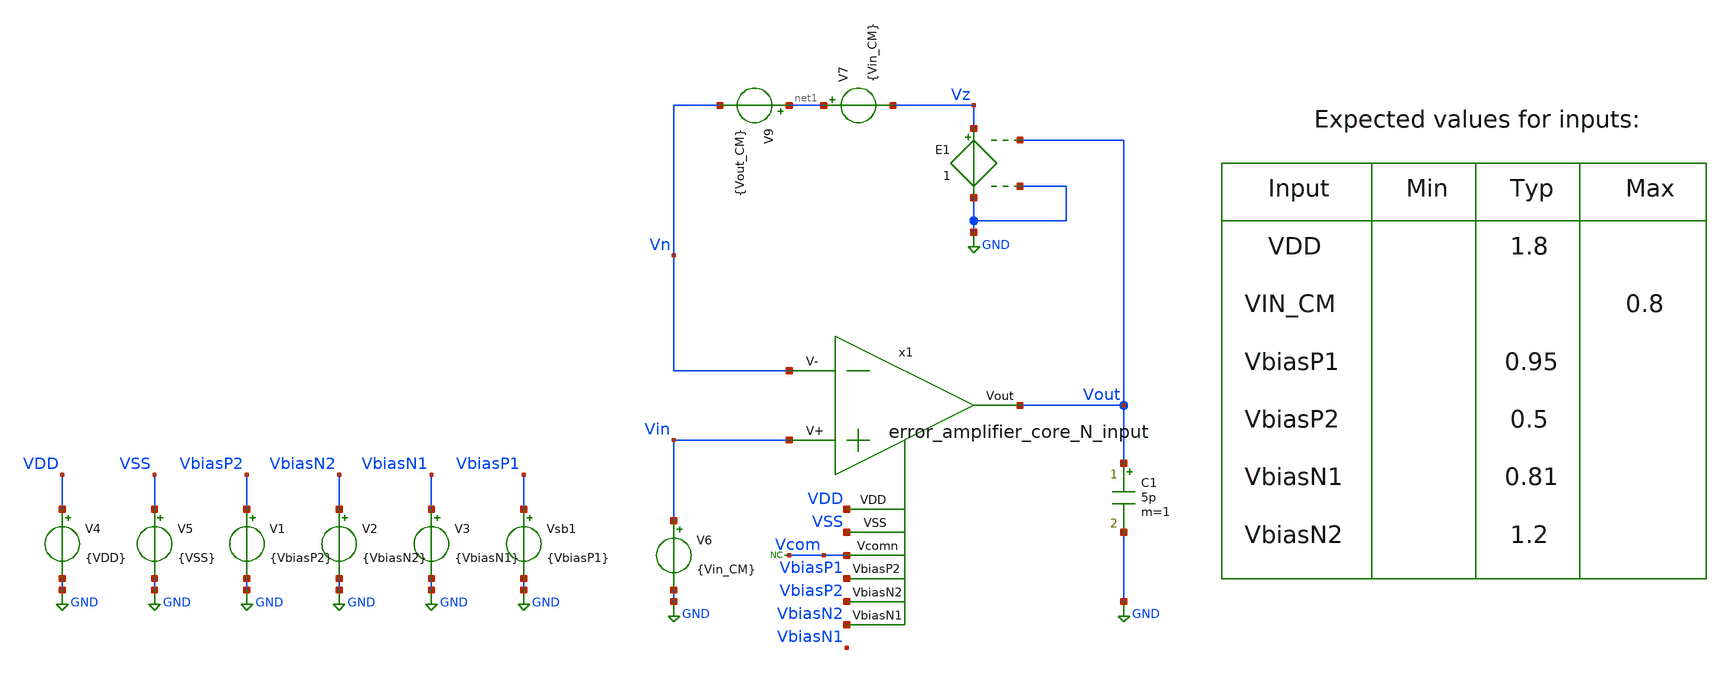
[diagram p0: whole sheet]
** sch_path: blocks/composite/folded_cascode/designs/gf180/error_amplifier_core_N_input/xschem/error_amplifier_core_Out_Swing.sch
**.subckt error_amplifier_core_Out_Swing
V1 VbiasP2 GND {VbiasP2}
V2 VbiasN2 GND {VbiasN2}
V3 VbiasN1 GND {VbiasN1}
V4 VDD GND {VDD}
V5 VSS GND {VSS}
C1 Vout GND 5p m=1
V6 Vin GND {Vin_CM}
x1 VbiasP1 VbiasP2 VbiasN2 Vout Vin Vn VDD VSS Vcom error_amplifier_core_N_input
Vsb1 VbiasP1 GND {VbiasP1}
V9 net1 Vn {Vout_CM}
E1 Vz GND Vout GND 1
* noconn Vcom
V7 net1 Vz {Vin_CM}
**** begin user architecture code




* --- Include PDK and Model Files ---
.include /foss/pdks/gf180mcuD/libs.tech/ngspice/design.ngspice
.lib /foss/pdks/gf180mcuD/libs.tech/ngspice/sm141064.ngspice typical

* --- Define Parameters for the Simulation ---
.param VDD = 1.8
.param VSS = 0
.param VbiasN1 = 0.81
.param VbiasN2 = 1.2
.param VbiasP1 = 0.95
.param VbiasP2 = 0.5
.param Vin_CM = 0.8
.param Vout_CM = 0.9
.param Vy = (Vout_CM - Vin_CM)
.param load_cap = 5*1e-12

* --- Simulation Commands and Analysis ---
.control
save all

** OP & DC simulations
op
dc V9 0 1.8 0.001

** DC measurements
setplot dc1
let dvout = deriv(v(Vout))

meas dc limmin when dvout=0.98 rise=1
meas dc limmax when dvout=0.98 fall=1

let Output_swing = limmax - limmin

print Output_swing
plot dvout


write error_amplifier_core_N_input_op.raw
.endc



**** end user architecture code
**.ends

* expanding   symbol:  gf180/error_amplifier_core_N_input/xschem/error_amplifier_core_N_input.sym #
*+ of pins=9
** sym_path: blocks/composite/folded_cascode/designs/gf180/error_amplifier_core_N_input/xschem/error_amplifier_core_N_input.sym
** sch_path: blocks/composite/folded_cascode/designs/gf180/error_amplifier_core_N_input/xschem/error_amplifier_core_N_input.sch
.subckt error_amplifier_core_N_input VbiasP2 VbiasN2 VbiasN1 Vout V+ V- VDD VSS Vcomn
*.ipin VbiasN2
*.iopin VDD
*.ipin VbiasP2
*.ipin VbiasN1
*.ipin V+
*.ipin V-
*.iopin VSS
*.iopin Vcomn
*.iopin Vout
XM4 Vdm6 Val VDD VDD pfet_03v3 L=0.3u W=4u nf=1 ad='int((nf+1)/2) * W/nf * 0.18u' as='int((nf+2)/2) * W/nf * 0.18u'
+ pd='2*int((nf+1)/2) * (W/nf + 0.18u)' ps='2*int((nf+2)/2) * (W/nf + 0.18u)' nrd='0.18u / W' nrs='0.18u / W'
+ sa=0 sb=0 sd=0 m=12
XM3 Vdm5 Val VDD VDD pfet_03v3 L=0.3u W=4u nf=1 ad='int((nf+1)/2) * W/nf * 0.18u' as='int((nf+2)/2) * W/nf * 0.18u'
+ pd='2*int((nf+1)/2) * (W/nf + 0.18u)' ps='2*int((nf+2)/2) * (W/nf + 0.18u)' nrd='0.18u / W' nrs='0.18u / W'
+ sa=0 sb=0 sd=0 m=12
XM5 Val VbiasP2 Vdm5 VDD pfet_03v3 L=2u W=6u nf=1 ad='int((nf+1)/2) * W/nf * 0.18u' as='int((nf+2)/2) * W/nf * 0.18u'
+ pd='2*int((nf+1)/2) * (W/nf + 0.18u)' ps='2*int((nf+2)/2) * (W/nf + 0.18u)' nrd='0.18u / W' nrs='0.18u / W'
+ sa=0 sb=0 sd=0 m=2
XM6 Vout VbiasP2 Vdm6 VDD pfet_03v3 L=2u W=6u nf=1 ad='int((nf+1)/2) * W/nf * 0.18u' as='int((nf+2)/2) * W/nf * 0.18u'
+ pd='2*int((nf+1)/2) * (W/nf + 0.18u)' ps='2*int((nf+2)/2) * (W/nf + 0.18u)' nrd='0.18u / W' nrs='0.18u / W'
+ sa=0 sb=0 sd=0 m=2
XM9 net1 VbiasN1 VSS VSS nfet_03v3 L=2u W=2u nf=1 ad='int((nf+1)/2) * W/nf * 0.18u' as='int((nf+2)/2) * W/nf * 0.18u'
+ pd='2*int((nf+1)/2) * (W/nf + 0.18u)' ps='2*int((nf+2)/2) * (W/nf + 0.18u)' nrd='0.18u / W' nrs='0.18u / W'
+ sa=0 sb=0 sd=0 m=2
XM8 Vout VbiasN2 Vcomn VSS nfet_03v3 L=2u W=5u nf=1 ad='int((nf+1)/2) * W/nf * 0.18u' as='int((nf+2)/2) * W/nf * 0.18u'
+ pd='2*int((nf+1)/2) * (W/nf + 0.18u)' ps='2*int((nf+2)/2) * (W/nf + 0.18u)' nrd='0.18u / W' nrs='0.18u / W'
+ sa=0 sb=0 sd=0 m=1
XM7 Val VbiasN2 net1 VSS nfet_03v3 L=2u W=5u nf=1 ad='int((nf+1)/2) * W/nf * 0.18u' as='int((nf+2)/2) * W/nf * 0.18u'
+ pd='2*int((nf+1)/2) * (W/nf + 0.18u)' ps='2*int((nf+2)/2) * (W/nf + 0.18u)' nrd='0.18u / W' nrs='0.18u / W'
+ sa=0 sb=0 sd=0 m=1
XM10 Vcomn VbiasN1 VSS VSS nfet_03v3 L=2u W=2u nf=1 ad='int((nf+1)/2) * W/nf * 0.18u' as='int((nf+2)/2) * W/nf * 0.18u'
+ pd='2*int((nf+1)/2) * (W/nf + 0.18u)' ps='2*int((nf+2)/2) * (W/nf + 0.18u)' nrd='0.18u / W' nrs='0.18u / W'
+ sa=0 sb=0 sd=0 m=2
XM15 VDD VDD VDD VDD pfet_03v3 L=3u W=1u nf=1 ad='int((nf+1)/2) * W/nf * 0.18u' as='int((nf+2)/2) * W/nf * 0.18u'
+ pd='2*int((nf+1)/2) * (W/nf + 0.18u)' ps='2*int((nf+2)/2) * (W/nf + 0.18u)' nrd='0.18u / W' nrs='0.18u / W'
+ sa=0 sb=0 sd=0 m=28
XM16 VDD VDD VDD VDD pfet_03v3 L=1.5u W=1u nf=1 ad='int((nf+1)/2) * W/nf * 0.18u' as='int((nf+2)/2) * W/nf * 0.18u'
+ pd='2*int((nf+1)/2) * (W/nf + 0.18u)' ps='2*int((nf+2)/2) * (W/nf + 0.18u)' nrd='0.18u / W' nrs='0.18u / W'
+ sa=0 sb=0 sd=0 m=20
XM13 VSS VSS VSS VSS nfet_03v3 L=3u W=1u nf=1 ad='int((nf+1)/2) * W/nf * 0.18u' as='int((nf+2)/2) * W/nf * 0.18u'
+ pd='2*int((nf+1)/2) * (W/nf + 0.18u)' ps='2*int((nf+2)/2) * (W/nf + 0.18u)' nrd='0.18u / W' nrs='0.18u / W'
+ sa=0 sb=0 sd=0 m=18
XM12 VSS VSS VSS VSS nfet_03v3 L=6.5u W=0.5u nf=1 ad='int((nf+1)/2) * W/nf * 0.18u' as='int((nf+2)/2) * W/nf * 0.18u'
+ pd='2*int((nf+1)/2) * (W/nf + 0.18u)' ps='2*int((nf+2)/2) * (W/nf + 0.18u)' nrd='0.18u / W' nrs='0.18u / W'
+ sa=0 sb=0 sd=0 m=36
XM14 VSS VSS VSS VSS nfet_03v3 L=1u W=1u nf=1 ad='int((nf+1)/2) * W/nf * 0.18u' as='int((nf+2)/2) * W/nf * 0.18u'
+ pd='2*int((nf+1)/2) * (W/nf + 0.18u)' ps='2*int((nf+2)/2) * (W/nf + 0.18u)' nrd='0.18u / W' nrs='0.18u / W'
+ sa=0 sb=0 sd=0 m=30
XM1 Vdm6 V- net2 VSS nfet_03v3 L=1u W=10u nf=1 ad='int((nf+1)/2) * W/nf * 0.18u' as='int((nf+2)/2) * W/nf * 0.18u'
+ pd='2*int((nf+1)/2) * (W/nf + 0.18u)' ps='2*int((nf+2)/2) * (W/nf + 0.18u)' nrd='0.18u / W' nrs='0.18u / W'
+ sa=0 sb=0 sd=0 m=20
XM2 Vdm5 V+ net2 VSS nfet_03v3 L=1u W=10u nf=1 ad='int((nf+1)/2) * W/nf * 0.18u' as='int((nf+2)/2) * W/nf * 0.18u'
+ pd='2*int((nf+1)/2) * (W/nf + 0.18u)' ps='2*int((nf+2)/2) * (W/nf + 0.18u)' nrd='0.18u / W' nrs='0.18u / W'
+ sa=0 sb=0 sd=0 m=20
XM11 net2 VbiasN1 VSS VSS nfet_03v3 L=2u W=2u nf=1 ad='int((nf+1)/2) * W/nf * 0.18u' as='int((nf+2)/2) * W/nf * 0.18u'
+ pd='2*int((nf+1)/2) * (W/nf + 0.18u)' ps='2*int((nf+2)/2) * (W/nf + 0.18u)' nrd='0.18u / W' nrs='0.18u / W'
+ sa=0 sb=0 sd=0 m=40
.ends

.GLOBAL GND
.end
